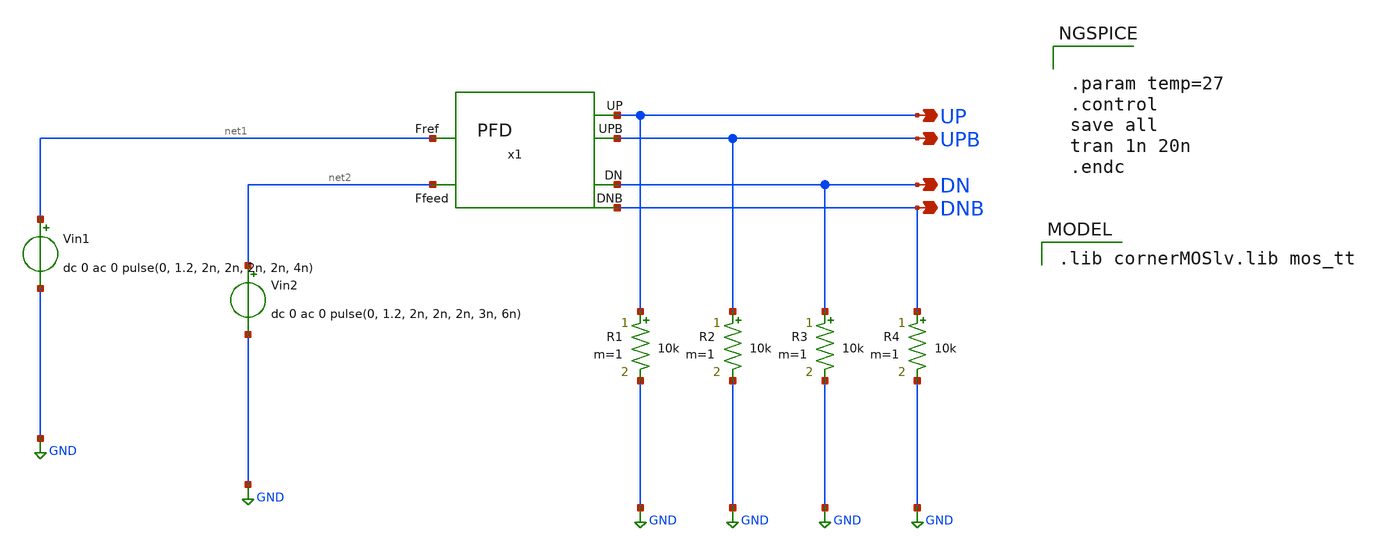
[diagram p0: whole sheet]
** sch_path: Team 1 Design/design_data/xschem/PFD/PFD_tb.sch
**.subckt PFD_tb UP UPB DN DNB
*.opin UP
*.opin UPB
*.opin DN
*.opin DNB
Vin1 net1 GND dc 0 ac 0 pulse(0, 1.2, 2n, 2n, 2n, 2n, 4n)
Vin2 net2 GND dc 0 ac 0 pulse(0, 1.2, 2n, 2n, 2n, 3n, 6n)
x1 net1 UP UPB DN DNB net2 PFD
R1 UP GND 10k m=1
R2 UPB GND 10k m=1
R3 DN GND 10k m=1
R4 DNB GND 10k m=1
**** begin user architecture code
 .lib cornerMOSlv.lib mos_tt



.param temp=27
.control
save all
tran 1n 20n
.endc


**** end user architecture code
**.ends
.GLOBAL GND
.end
